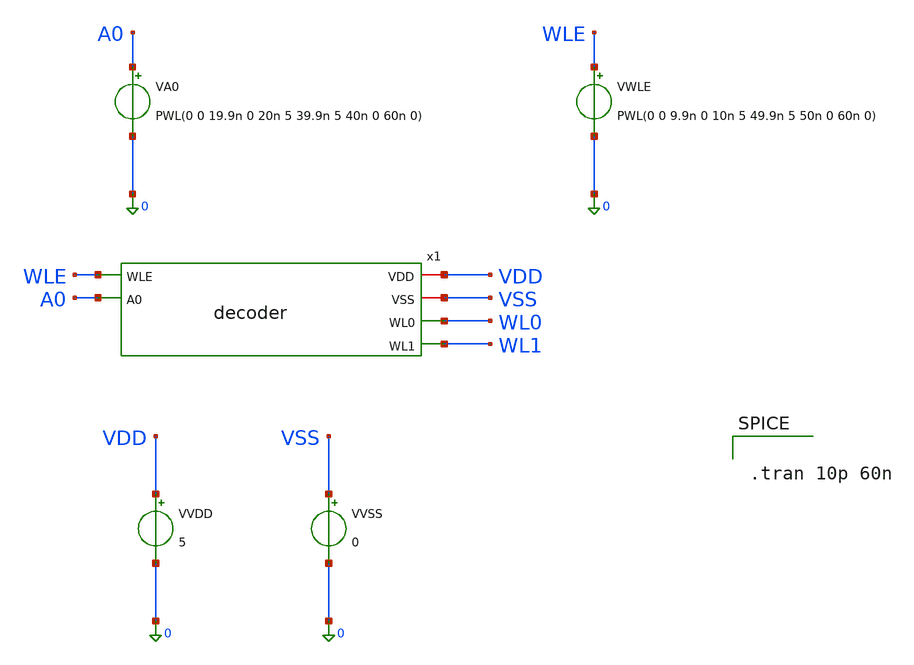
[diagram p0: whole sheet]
** sch_path: Deliverables/tb_decoder.sch
**.subckt tb_decoder
VA0 A0 0 PWL(0 0 19.9n 0 20n 5 39.9n 5 40n 0 60n 0)
VVDD VDD 0 5
VVSS VSS 0 0
x1 VDD VSS WL0 WLE A0 WL1 decoder
VWLE WLE 0 PWL(0 0 9.9n 0 10n 5 49.9n 5 50n 0 60n 0)
**** begin user architecture code
 .include $::LIB/ip62_models


.tran 10p 60n



**** end user architecture code
**.ends
.end
